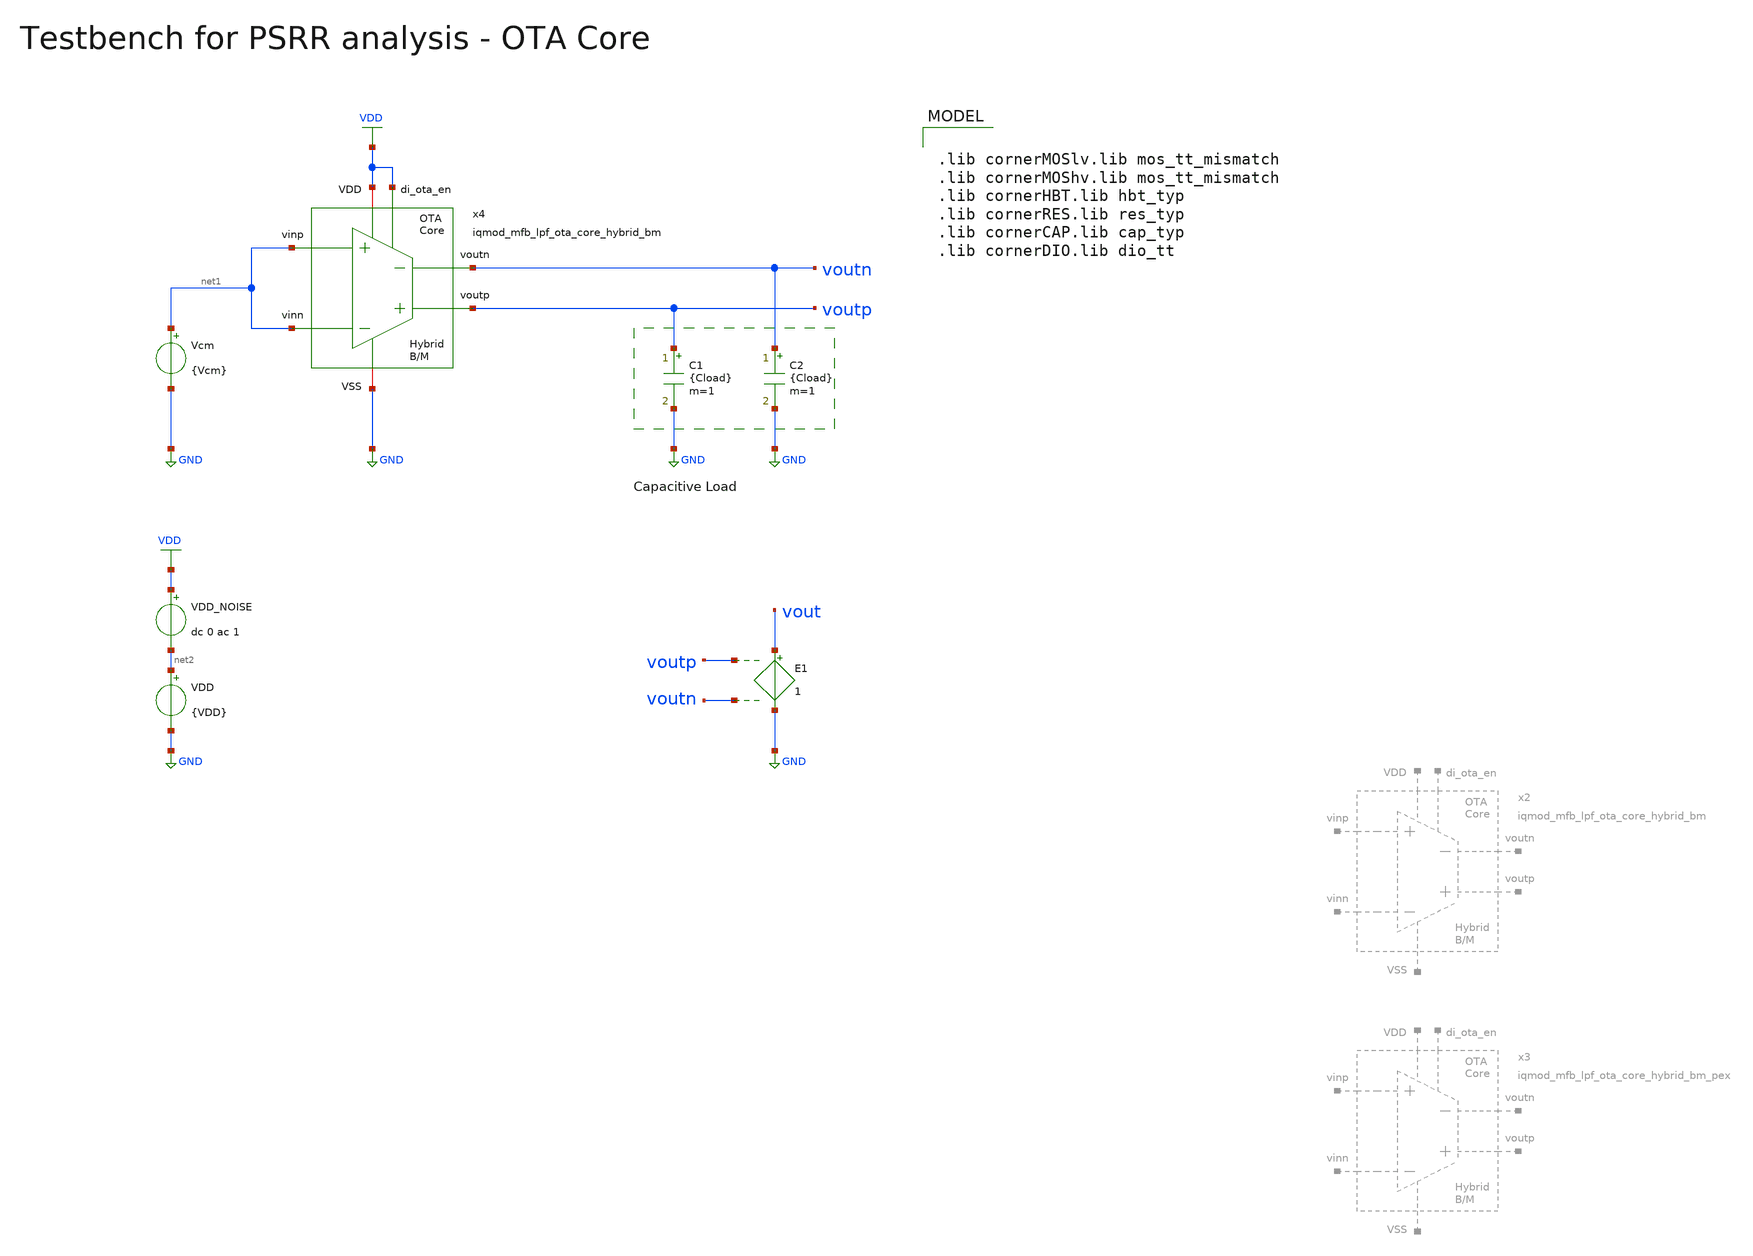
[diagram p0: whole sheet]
** sch_path: ihp130/macros/iqmod/xschem/testbenches/iqmod_mfb_lpf_ota_core_tb_PSRR.sch
**.subckt iqmod_mfb_lpf_ota_core_tb_PSRR
C1 voutp GND {Cload} m=1
C2 voutn GND {Cload} m=1
Vcm net1 GND {Vcm}
E1 vout GND voutp voutn 1
VDD net2 GND {VDD}
VDD_NOISE VDD net2 dc 0 ac 1
x4 voutp voutn net1 net1 VDD GND VDD iqmod_mfb_lpf_ota_core_hybrid_bm
**** begin user architecture code


*.include ../../spice/iqmod_mfb_lpf_ota_core_hybrid_bm_pex.spice
.param VDD=1.5
.param Vcm=VDD/2
.param temp=27
.param Cload=10p
.options savecurrents klu method=gear reltol=1e-4 abstol=1e-15 gmin=1e-15
.control

* save v(VDD) v(vout) v(voutp) v(voutn)
save all

set wr_vecnames
set wr_singlescale

* User Constants
let f_min = 0.1
let f_max = 1G
let fdc = 1

* Operating Point Analysis
op
remzerovec
write iqmod_mfb_lpf_ota_core_tb_PSRR.raw
set appendwrite

* AC Analysis
ac dec 101 $&const.f_min $&const.f_max
remzerovec
write iqmod_mfb_lpf_ota_core_tb_PSRR.raw

* Plotting
let PSRR = v(VDD)/v(vout)
let PSRRp = v(VDD)/v(voutp)
let PSRRn = v(VDD)/v(voutn)

let PSRR_dB = vdb(PSRR)
let PSRRp_dB = vdb(PSRRp)
let PSRRn_dB = vdb(PSRRn)

plot PSRR_dB PSRRp_dB PSRRn_dB ylabel 'PSRR, PSRR+, PSRR-'

* Measurements
meas ac PSRRdc_dB find PSRR_dB when frequency = fdc
print PSRRdc_dB

meas ac PSRRpdc_dB find PSRRp_dB when frequency = fdc
print PSRRpdc_dB

meas ac PSRRndc_dB find PSRRn_dB when frequency = fdc
print PSRRndc_dB

* Write Data
unset appendwrite
set wr_vecnames
set wr_singlescale
wrdata $PROJECT_PATH/python/plot_simulations/data/iqmod_mfb_lpf_ota_core_tb_PSRR.txt v(PSRR_dB)

*quit
.endc



.lib cornerMOSlv.lib mos_tt_mismatch
.lib cornerMOShv.lib mos_tt_mismatch
.lib cornerHBT.lib hbt_typ
.lib cornerRES.lib res_typ
.lib cornerCAP.lib cap_typ
.lib cornerDIO.lib dio_tt

**** end user architecture code
**.ends
.GLOBAL GND
.GLOBAL VDD
.end
